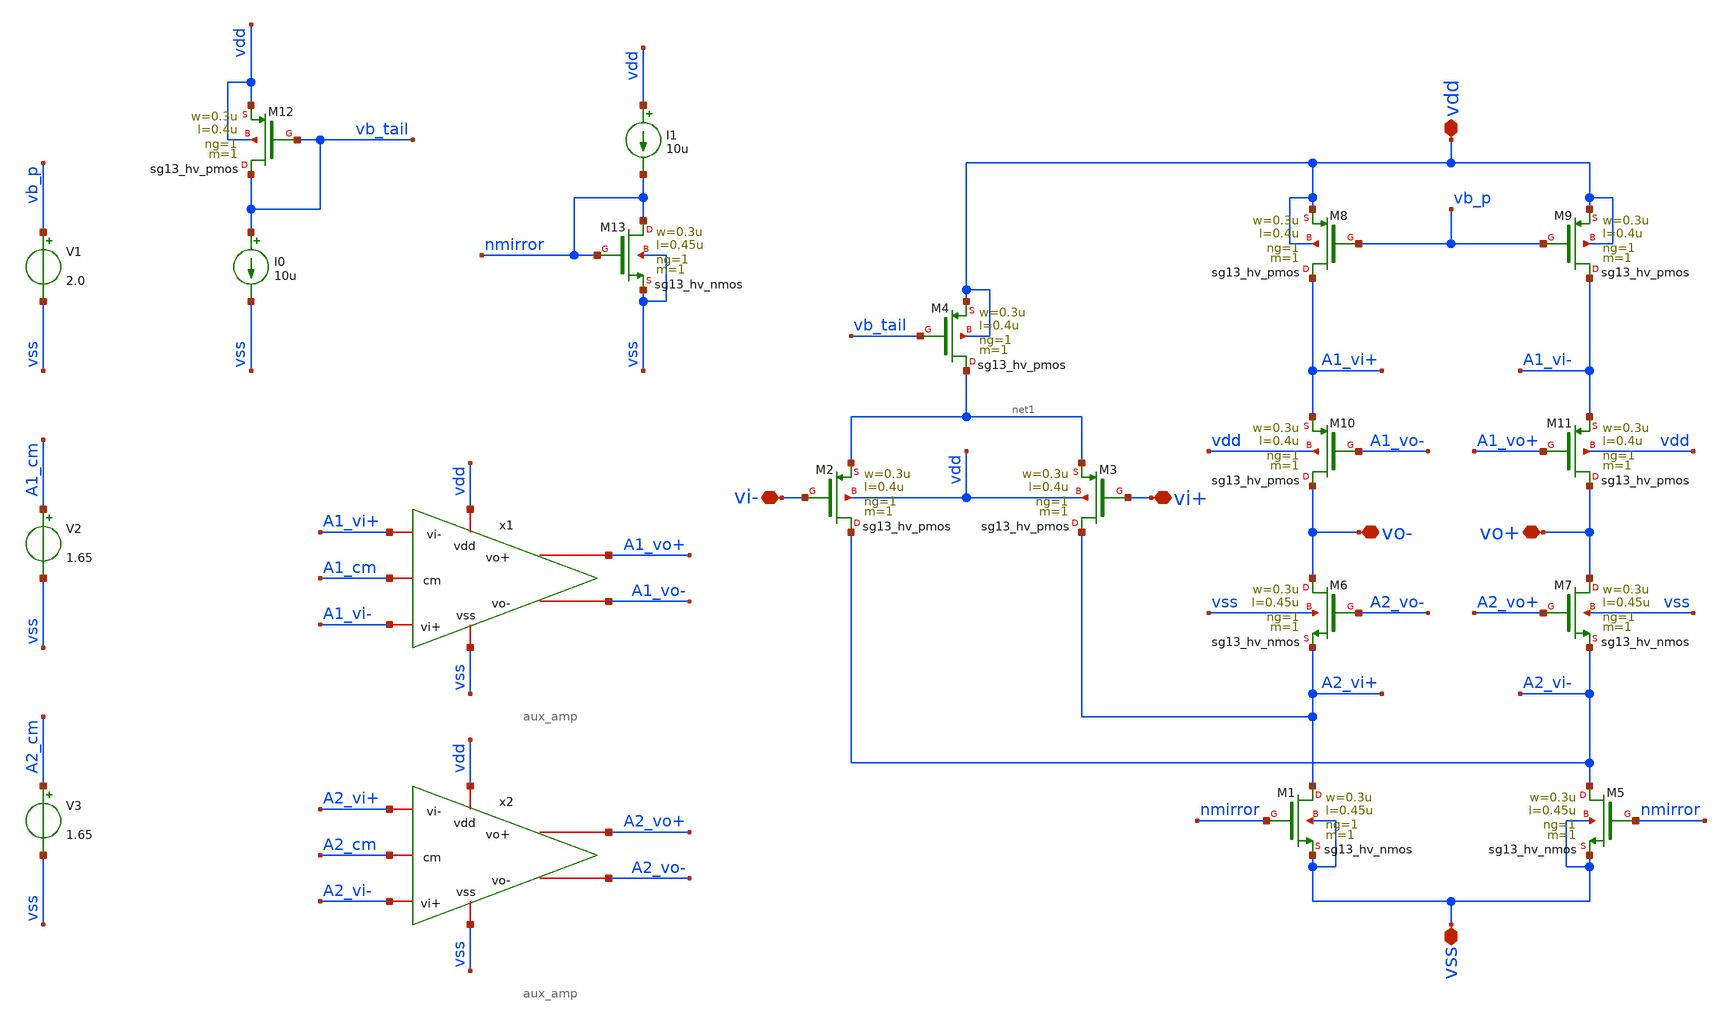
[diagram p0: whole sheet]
** sch_path: schematic/balaudio_amp.sch
**.subckt balaudio_amp vdd vss vi+ vi- vo- vo+
*.iopin vdd
*.iopin vss
*.iopin vi+
*.iopin vi-
*.iopin vo-
*.iopin vo+
XM1 A2_vi+ nmirror vss vss sg13_hv_nmos w=0.3u l=0.45u ng=1 m=1 mm_ok=1
XM2 A2_vi- vi- net1 vdd sg13_hv_pmos w=0.3u l=0.4u ng=1 m=1 mm_ok=1
XM3 A2_vi+ vi+ net1 vdd sg13_hv_pmos w=0.3u l=0.4u ng=1 m=1 mm_ok=1
XM4 net1 vb_tail vdd vdd sg13_hv_pmos w=0.3u l=0.4u ng=1 m=1 mm_ok=1
XM5 A2_vi- nmirror vss vss sg13_hv_nmos w=0.3u l=0.45u ng=1 m=1 mm_ok=1
XM6 vo- A2_vo- A2_vi+ vss sg13_hv_nmos w=0.3u l=0.45u ng=1 m=1 mm_ok=1
XM7 vo+ A2_vo+ A2_vi- vss sg13_hv_nmos w=0.3u l=0.45u ng=1 m=1 mm_ok=1
XM8 A1_vi+ vb_p vdd vdd sg13_hv_pmos w=0.3u l=0.4u ng=1 m=1 mm_ok=1
XM9 A1_vi- vb_p vdd vdd sg13_hv_pmos w=0.3u l=0.4u ng=1 m=1 mm_ok=1
XM10 vo- A1_vo- A1_vi+ vdd sg13_hv_pmos w=0.3u l=0.4u ng=1 m=1 mm_ok=1
XM11 vo+ A1_vo+ A1_vi- vdd sg13_hv_pmos w=0.3u l=0.4u ng=1 m=1 mm_ok=1
x1 vdd A1_vi+ A1_vi- A1_vo+ A1_vo- vss A1_cm aux_amp
x2 vdd A2_vi+ A2_vi- A2_vo+ A2_vo- vss A2_cm aux_amp
XM12 vb_tail vb_tail vdd vdd sg13_hv_pmos w=0.3u l=0.4u ng=1 m=1 mm_ok=1
I0 vb_tail vss 10u
V1 vb_p vss 2.0
XM13 nmirror nmirror vss vss sg13_hv_nmos w=0.3u l=0.45u ng=1 m=1 mm_ok=1
I1 vdd nmirror 10u
V2 A1_cm vss 1.65
V3 A2_cm vss 1.65
**.ends

* expanding   symbol:  aux_amp.sym # of pins=7
** sym_path: schematic/aux_amp.sym
** sch_path: schematic/aux_amp.sch
.subckt aux_amp vdd vi- vi+ vo+ vo- vss cm_in
*.iopin vss
*.iopin vo-
*.iopin vdd
*.iopin vo+
*.iopin vi-
*.iopin vi+
*.iopin cm_in
XM1 net3 vi+ net1 net1 sg13_hv_nmos w=80.0u l=10.0u ng=8 m=1 mm_ok=1
XM2 net4 cm_in net1 net1 sg13_hv_nmos w=80.0u l=10.0u ng=8 m=1 mm_ok=1
XM5 net1 nbias vss vss sg13_hv_nmos w=60.0u l=10.0u ng=8 m=1 mm_ok=1
XM3 net3 cm_in net2 net2 sg13_hv_nmos w=80.0u l=10.0u ng=8 m=1 mm_ok=1
XM4 net4 vi- net2 net2 sg13_hv_nmos w=80.0u l=10.0u ng=8 m=1 mm_ok=1
XM6 net2 nbias vss vss sg13_hv_nmos w=60.0u l=10.0u ng=8 m=1 mm_ok=1
XM11 vo- nbias vss vss sg13_hv_nmos w=29.0u l=10.0u ng=8 m=1 mm_ok=1
XM12 vo+ nbias vss vss sg13_hv_nmos w=29.0u l=10.0u ng=8 m=1 mm_ok=1
V3 pbias vss 1.80
XM9 vo- pbias net3 net3 sg13_hv_pmos w=15.0u l=2.0u ng=8 m=1 mm_ok=1
XM7 net3 pbias_top vdd vdd sg13_hv_pmos w=4.0u l=1.0u ng=1 m=1 mm_ok=1
XM8 net4 pbias_top vdd vdd sg13_hv_pmos w=4.0u l=1.0u ng=1 m=1 mm_ok=1
XM10 vo+ pbias net4 net4 sg13_hv_pmos w=15.0u l=2.0u ng=8 m=1 mm_ok=1
XM14 nbias nbias vss vss sg13_hv_nmos w=29.0u l=10.0u ng=8 m=1 mm_ok=1
I1 vdd nbias 1.0u
V1 pbias_top vss 2.2
.ends

.end
